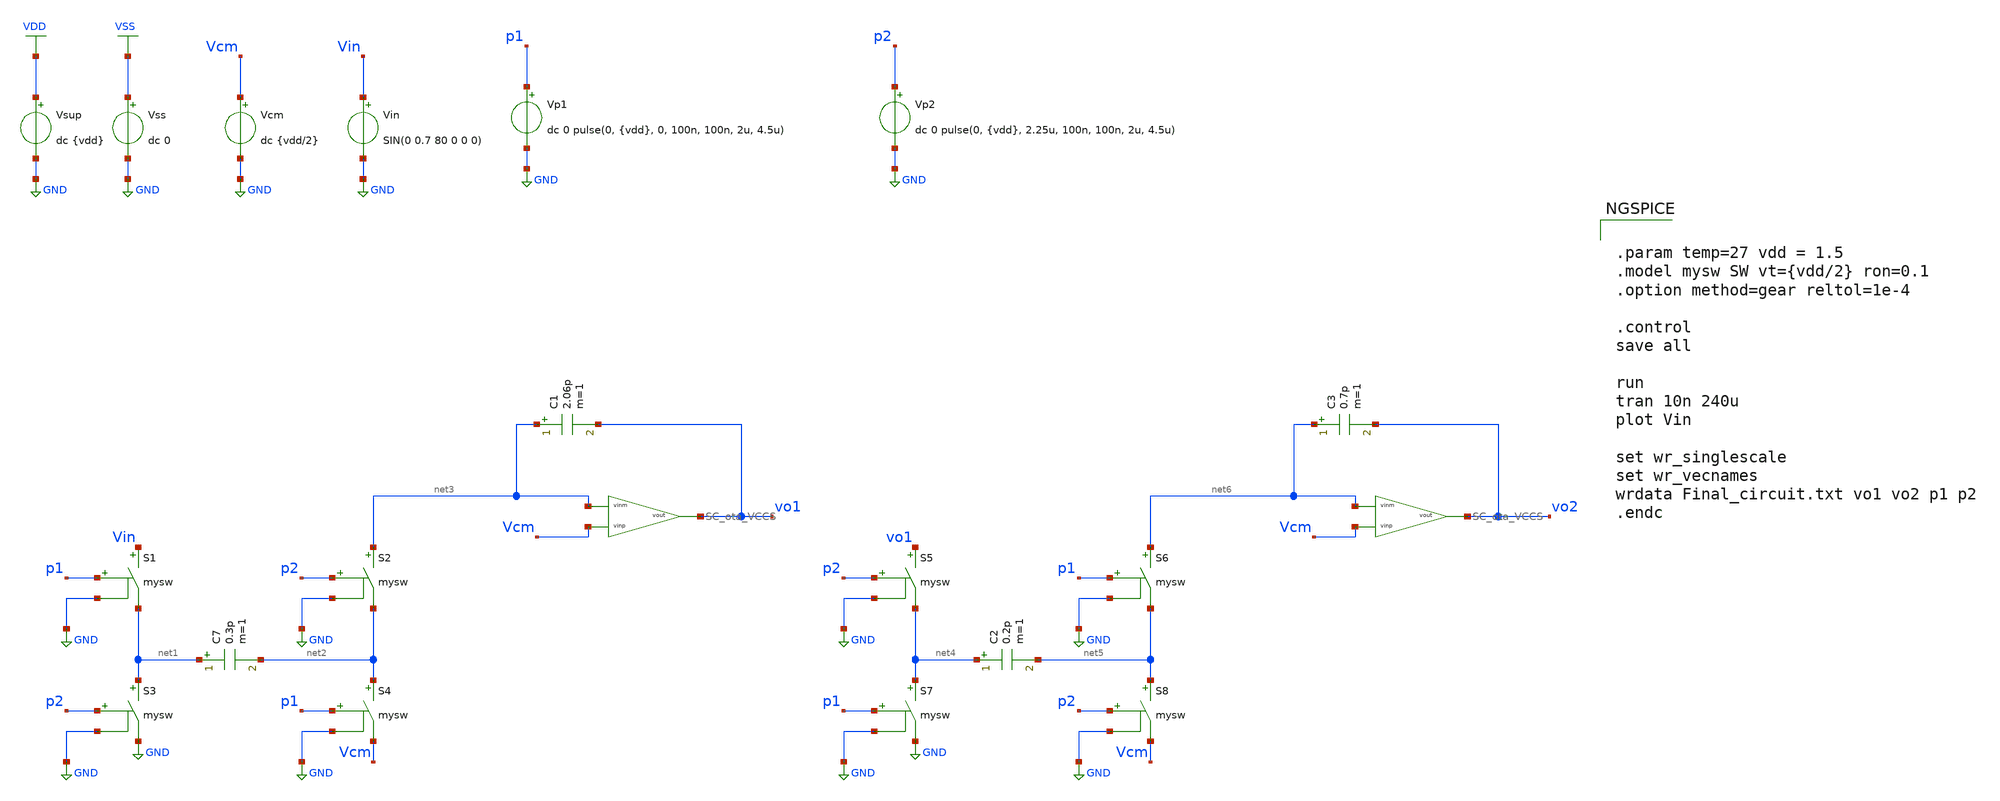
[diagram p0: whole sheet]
** sch_path: design/design_switch_cap/Final_circuit.sch
**.subckt Final_circuit
Vcm Vcm GND dc {vdd/2}
Vin Vin GND SIN(0 0.7 80 0 0 0)
S1 Vin net1 p1 GND mysw
S2 net3 net2 p2 GND mysw
S3 net1 GND p2 GND mysw
S4 net2 Vcm p1 GND mysw
C7 net1 net2 0.3p m=1
C1 net3 vo1 2.06p m=1
Vsup VDD GND dc {vdd}
Vss VSS GND dc 0
S5 vo1 net4 p2 GND mysw
S6 net6 net5 p1 GND mysw
S7 net4 GND p1 GND mysw
S8 net5 Vcm p2 GND mysw
C2 net4 net5 0.2p m=1
C3 net6 vo2 0.7p m=1
Vp1 p1 GND dc 0 pulse(0, {vdd}, 0, 100n, 100n, 2u, 4.5u)
Vp2 p2 GND dc 0 pulse(0, {vdd}, 2.25u, 100n, 100n, 2u, 4.5u)
x1 vo1 net3 Vcm SC_ota_VCCS
x2 vo2 net6 Vcm SC_ota_VCCS
**** begin user architecture code

.lib $::SG13G2_MODELS/cornerMOSlv.lib mos_tt
.lib $::SG13G2_MODELS/cornerRES.lib res_typ
.inc /foss/pdks/ihp-sg13g2/libs.ref/sg13g2_stdcell/spice/sg13g2_stdcell.spice



.param temp=27 vdd = 1.5
.model mysw SW vt={vdd/2} ron=0.1
.option method=gear reltol=1e-4

.control
save all

run
tran 10n 240u
plot Vin

set wr_singlescale
set wr_vecnames
wrdata Final_circuit.txt vo1 vo2 p1 p2
.endc


**** end user architecture code
**.ends
.GLOBAL GND
.GLOBAL VDD
.GLOBAL VSS
.end
